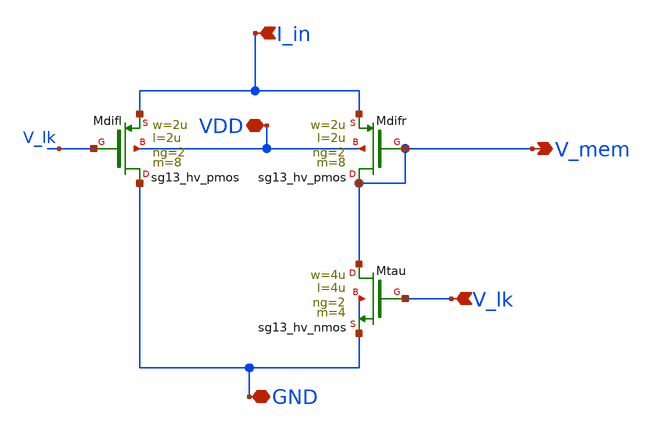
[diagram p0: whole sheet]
** sch_path: xschem/DPI.sch
**.subckt DPI V_mem V_lk I_in VDD GND
*.opin V_mem
*.ipin V_lk
*.ipin I_in
*.iopin VDD
*.iopin GND
XMdifl GND V_lk I_in VDD sg13_hv_pmos w=2u l=2u ng=2 m=8 mm_ok=1
XMdifr V_mem V_mem I_in VDD sg13_hv_pmos w=2u l=2u ng=2 m=8 mm_ok=1
XMtau V_mem V_lk GND GND sg13_hv_nmos w=4u l=4u ng=2 m=4 mm_ok=1
**.ends
.end
